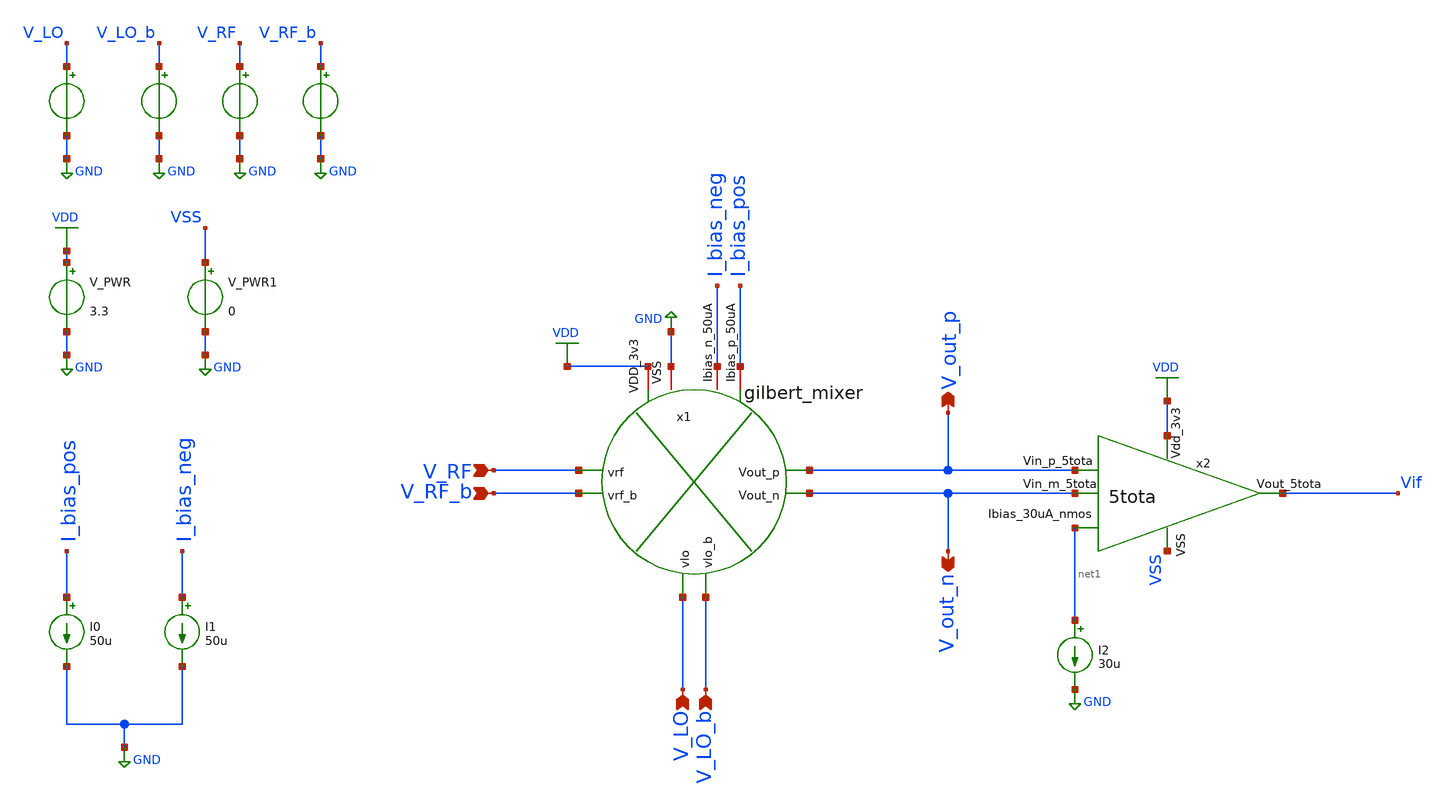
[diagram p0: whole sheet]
** sch_path: Analog/schematics/2_mixer/mixer_tb_without_lpf.sch
**.subckt mixer_tb_without_lpf V_LO V_LO_b V_RF V_RF_b V_out_p V_out_n
*.ipin V_LO
*.ipin V_LO_b
*.ipin V_RF
*.ipin V_RF_b
*.opin V_out_p
*.opin V_out_n
I2 net1 GND 30u
V_PWR VDD GND 3.3
.save i(v_pwr)
V_LO V_LO GND pulse(0 1.5 0 1p 1p 0.25n 0.5n)
.save i(v_lo)
V_LO_b V_LO_b GND pulse(0 1.5 0 1p 1p 0.25n 0.5n)
.save i(v_lo_b)
V_RF V_RF GND sin( 1 1 1 0 )
.save i(v_rf)
V_RF_b V_RF_b GND sin( 1 1 1 0 0 180 )
.save i(v_rf_b)
I0 I_bias_pos GND 50u
I1 I_bias_neg GND 50u
V_PWR1 VSS GND 0
.save i(v_pwr1)
x1 V_out_n V_out_p V_LO V_LO_b V_RF V_RF_b I_bias_neg I_bias_pos GND VDD gilbert_mixer
x2 VDD Vif V_out_p V_out_n VSS net1 5tota
**** begin user architecture code

.include $::180MCU_MODELS/design.ngspice
.lib $::180MCU_MODELS/sm141064.ngspice typical
.lib $::180MCU_MODELS/sm141064.ngspice mimcap_typical
.lib $::180MCU_MODELS/sm141064.ngspice cap_mim
.lib $::180MCU_MODELS/sm141064.ngspice res_typical




* let sets vectors to a plot, while set sets a variable, globally accessible in .control
.control

    * Set frequency and amplitude variables to proper values from within the control sequence
    * sine-wave LO
    * set cm_lo = 0.5
    * set freq_lo = 2.50G
    * set amp_lo = 0.5
    * alter @V_LO[sin] = [ $cm_lo $amp_lo $freq_lo 0 ]
    * alter @V_LO_b[sin] = [ $cm_lo $amp_lo $freq_lo 0 0 180 ]

    set freq_lo = 156k
    set cm_lo = 1.8
    set amp_lo = 0.4

    set cm_rf  = 1.2
    set freq_rf = 156k
    * set freq_rf = 10.7Meg
    set amp_rf  = 0.1

    * set the parameters to the voltage sources
    * alter @V_LO[pulse] = [ 2 2.5 0 0.5p 0.5p 5n 10n ]
    * alter @V_LO_b[pulse] = [ 2 2.5 5n 0.5p 0.5p 5n 10n]
    alter @V_LO[sin] = [ $cm_lo $amp_lo $freq_lo 0 ]
    alter @V_LO_b[sin] = [ $cm_lo $amp_lo $freq_lo 0 0 180 ]
    alter @V_RF[sin] = [ $cm_rf $amp_rf $freq_rf 0 ]
    alter @V_RF_b[sin] = [ $cm_rf $amp_rf $freq_rf 0 0 180 ]

    save all

    tran 100p 2m

    let if_out = v(v_out_p) - v(v_out_n)
    let vlo = v(v_lo) - v(v_lo_b)
    let vrf = v(v_rf) - v(v_rf_b)

    linearize v(vif) vlo vrf

    fft v(vif) vlo vrf

    let vlo_db = db(mag(vlo))
    let vrf_db = db(mag(vrf))
    let vif_db = db(mag(v(vif)))

    plot vlo_db vrf_db vif_db xlimit 0 400k

    write /workspace/Analog/schematics/2_mixer/simulation_files/mixer_tb.raw

.endc


**** end user architecture code
**.ends
.GLOBAL GND
.GLOBAL VDD
.end
